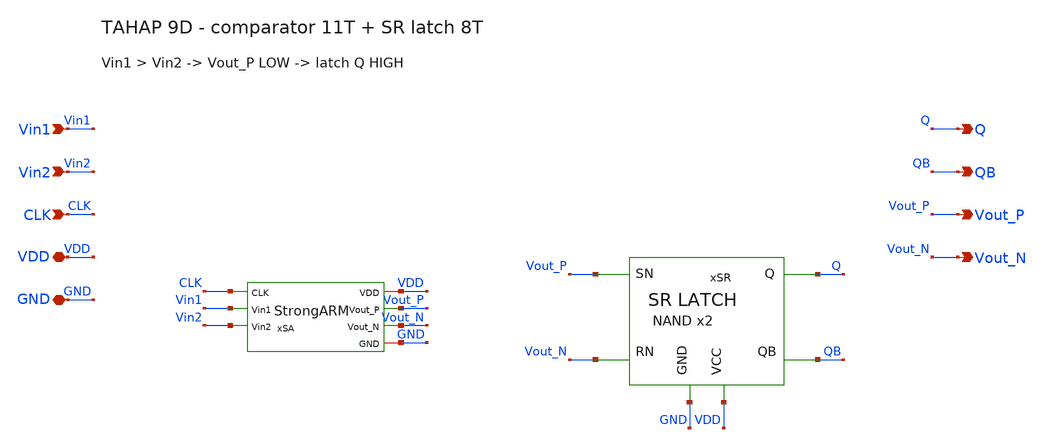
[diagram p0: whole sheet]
** sch_path: blocks/03_StrongARM/xschem/StrongARM_Latch.sch
**.subckt StrongARM_Latch Vin1 Vin2 CLK VDD GND Q QB Vout_P Vout_N
*.ipin Vin1
*.ipin Vin2
*.ipin CLK
*.iopin VDD
*.iopin GND
*.opin Q
*.opin QB
*.opin Vout_P
*.opin Vout_N
xSA VDD CLK Vout_P Vout_N Vin1 Vin2 GND StrongARM
xSR Vout_P Vout_N Q QB GND VDD SR_Latch
**.ends

* expanding   symbol:  blocks/03_StrongARM/xschem/StrongARM.sym # of pins=7
** sym_path: blocks/03_StrongARM/xschem/StrongARM.sym
** sch_path: blocks/03_StrongARM/xschem/StrongARM.sch
.subckt StrongARM VDD CLK Vout_P Vout_N Vin1 Vin2 GND
*.iopin VDD
*.iopin GND
*.ipin Vin1
*.ipin Vin2
*.ipin CLK
*.opin Vout_P
*.opin Vout_N
XS1 P CLK VDD VDD sky130_fd_pr__pfet_01v8 L=0.15 W=1.5 nf=1 ad='int((1 + 1)/2) * 1.5 / 1 * 0.29' as='int((1 + 2)/2) * 1.5 / 1 * 0.29'
+ pd='2*int((1 + 1)/2) * (1.5 / 1 + 0.29)' ps='2*int((1 + 2)/2) * (1.5 / 1 + 0.29)' nrd='0.29 / 1.5 ' nrs='0.29 / 1.5 '
+ sa=0 sb=0 sd=0 mult=1 m=1
XS3 Vout_P CLK VDD VDD sky130_fd_pr__pfet_01v8 L=0.15 W=1.5 nf=1 ad='int((1 + 1)/2) * 1.5 / 1 * 0.29'
+ as='int((1 + 2)/2) * 1.5 / 1 * 0.29' pd='2*int((1 + 1)/2) * (1.5 / 1 + 0.29)' ps='2*int((1 + 2)/2) * (1.5 / 1 + 0.29)'
+ nrd='0.29 / 1.5 ' nrs='0.29 / 1.5 ' sa=0 sb=0 sd=0 mult=1 m=1
XM5 Vout_P Vout_N VDD VDD sky130_fd_pr__pfet_01v8 L=0.3 W=5 nf=1 ad='int((1 + 1)/2) * 5 / 1 * 0.29' as='int((1 + 2)/2) * 5 / 1 * 0.29'
+ pd='2*int((1 + 1)/2) * (5 / 1 + 0.29)' ps='2*int((1 + 2)/2) * (5 / 1 + 0.29)' nrd='0.29 / 5 ' nrs='0.29 / 5 '
+ sa=0 sb=0 sd=0 mult=1 m=1
XM6 Vout_N Vout_P VDD VDD sky130_fd_pr__pfet_01v8 L=0.3 W=5 nf=1 ad='int((1 + 1)/2) * 5 / 1 * 0.29' as='int((1 + 2)/2) * 5 / 1 * 0.29'
+ pd='2*int((1 + 1)/2) * (5 / 1 + 0.29)' ps='2*int((1 + 2)/2) * (5 / 1 + 0.29)' nrd='0.29 / 5 ' nrs='0.29 / 5 '
+ sa=0 sb=0 sd=0 mult=1 m=1
XS4 Vout_N CLK VDD VDD sky130_fd_pr__pfet_01v8 L=0.15 W=1.5 nf=1 ad='int((1 + 1)/2) * 1.5 / 1 * 0.29'
+ as='int((1 + 2)/2) * 1.5 / 1 * 0.29' pd='2*int((1 + 1)/2) * (1.5 / 1 + 0.29)' ps='2*int((1 + 2)/2) * (1.5 / 1 + 0.29)'
+ nrd='0.29 / 1.5 ' nrs='0.29 / 1.5 ' sa=0 sb=0 sd=0 mult=1 m=1
XS2 Q CLK VDD VDD sky130_fd_pr__pfet_01v8 L=0.15 W=1.5 nf=1 ad='int((1 + 1)/2) * 1.5 / 1 * 0.29' as='int((1 + 2)/2) * 1.5 / 1 * 0.29'
+ pd='2*int((1 + 1)/2) * (1.5 / 1 + 0.29)' ps='2*int((1 + 2)/2) * (1.5 / 1 + 0.29)' nrd='0.29 / 1.5 ' nrs='0.29 / 1.5 '
+ sa=0 sb=0 sd=0 mult=1 m=1
XM3 Vout_P Vout_N P GND sky130_fd_pr__nfet_01v8 L=0.3 W=2 nf=1 ad='int((1 + 1)/2) * 2 / 1 * 0.29' as='int((1 + 2)/2) * 2 / 1 * 0.29'
+ pd='2*int((1 + 1)/2) * (2 / 1 + 0.29)' ps='2*int((1 + 2)/2) * (2 / 1 + 0.29)' nrd='0.29 / 2 ' nrs='0.29 / 2 '
+ sa=0 sb=0 sd=0 mult=1 m=1
XM4 Vout_N Vout_P Q GND sky130_fd_pr__nfet_01v8 L=0.3 W=2 nf=1 ad='int((1 + 1)/2) * 2 / 1 * 0.29' as='int((1 + 2)/2) * 2 / 1 * 0.29'
+ pd='2*int((1 + 1)/2) * (2 / 1 + 0.29)' ps='2*int((1 + 2)/2) * (2 / 1 + 0.29)' nrd='0.29 / 2 ' nrs='0.29 / 2 '
+ sa=0 sb=0 sd=0 mult=1 m=1
XM1 P Vin1 TAIL GND sky130_fd_pr__nfet_01v8 L=0.5 W=10 nf=1 ad='int((1 + 1)/2) * 10 / 1 * 0.29' as='int((1 + 2)/2) * 10 / 1 * 0.29'
+ pd='2*int((1 + 1)/2) * (10 / 1 + 0.29)' ps='2*int((1 + 2)/2) * (10 / 1 + 0.29)' nrd='0.29 / 10 ' nrs='0.29 / 10 '
+ sa=0 sb=0 sd=0 mult=1 m=1
XM2 Q Vin2 TAIL GND sky130_fd_pr__nfet_01v8 L=0.5 W=10 nf=1 ad='int((1 + 1)/2) * 10 / 1 * 0.29' as='int((1 + 2)/2) * 10 / 1 * 0.29'
+ pd='2*int((1 + 1)/2) * (10 / 1 + 0.29)' ps='2*int((1 + 2)/2) * (10 / 1 + 0.29)' nrd='0.29 / 10 ' nrs='0.29 / 10 '
+ sa=0 sb=0 sd=0 mult=1 m=1
XM7 TAIL CLK GND GND sky130_fd_pr__nfet_01v8 L=0.3 W=1 nf=1 ad='int((1 + 1)/2) * 1 / 1 * 0.29' as='int((1 + 2)/2) * 1 / 1 * 0.29'
+ pd='2*int((1 + 1)/2) * (1 / 1 + 0.29)' ps='2*int((1 + 2)/2) * (1 / 1 + 0.29)' nrd='0.29 / 1 ' nrs='0.29 / 1 '
+ sa=0 sb=0 sd=0 mult=1 m=1
.ends


* expanding   symbol:  blocks/03_StrongARM/xschem/SR_Latch.sym # of pins=6
** sym_path: blocks/03_StrongARM/xschem/SR_Latch.sym
** sch_path: blocks/03_StrongARM/xschem/SR_Latch.sch
.subckt SR_Latch SN RN Q QB GND VCC
*.ipin SN
*.ipin RN
*.opin Q
*.opin QB
*.iopin VCC
*.iopin GND
x1 SN QB Q GND VCC NAND2
x2 RN Q QB GND VCC NAND2
.ends


* expanding   symbol:  blocks/03_StrongARM/xschem/NAND2.sym # of pins=5
** sym_path: blocks/03_StrongARM/xschem/NAND2.sym
** sch_path: blocks/03_StrongARM/xschem/NAND2.sch
.subckt NAND2 A B Y GND VCC
*.iopin VCC
*.iopin GND
*.ipin A
*.ipin B
*.opin Y
XM1 Y A VCC VCC sky130_fd_pr__pfet_01v8 L=0.15 W=2 nf=1 ad='int((1 + 1)/2) * 2 / 1 * 0.29' as='int((1 + 2)/2) * 2 / 1 * 0.29'
+ pd='2*int((1 + 1)/2) * (2 / 1 + 0.29)' ps='2*int((1 + 2)/2) * (2 / 1 + 0.29)' nrd='0.29 / 2 ' nrs='0.29 / 2 '
+ sa=0 sb=0 sd=0 mult=1 m=1
XM2 Y B VCC VCC sky130_fd_pr__pfet_01v8 L=0.15 W=2 nf=1 ad='int((1 + 1)/2) * 2 / 1 * 0.29' as='int((1 + 2)/2) * 2 / 1 * 0.29'
+ pd='2*int((1 + 1)/2) * (2 / 1 + 0.29)' ps='2*int((1 + 2)/2) * (2 / 1 + 0.29)' nrd='0.29 / 2 ' nrs='0.29 / 2 '
+ sa=0 sb=0 sd=0 mult=1 m=1
XM3 Y A net1 GND sky130_fd_pr__nfet_01v8 L=0.15 W=2 nf=1 ad='int((1 + 1)/2) * 2 / 1 * 0.29' as='int((1 + 2)/2) * 2 / 1 * 0.29'
+ pd='2*int((1 + 1)/2) * (2 / 1 + 0.29)' ps='2*int((1 + 2)/2) * (2 / 1 + 0.29)' nrd='0.29 / 2 ' nrs='0.29 / 2 '
+ sa=0 sb=0 sd=0 mult=1 m=1
XM4 net1 B GND GND sky130_fd_pr__nfet_01v8 L=0.15 W=2 nf=1 ad='int((1 + 1)/2) * 2 / 1 * 0.29' as='int((1 + 2)/2) * 2 / 1 * 0.29'
+ pd='2*int((1 + 1)/2) * (2 / 1 + 0.29)' ps='2*int((1 + 2)/2) * (2 / 1 + 0.29)' nrd='0.29 / 2 ' nrs='0.29 / 2 '
+ sa=0 sb=0 sd=0 mult=1 m=1
.ends

.end
